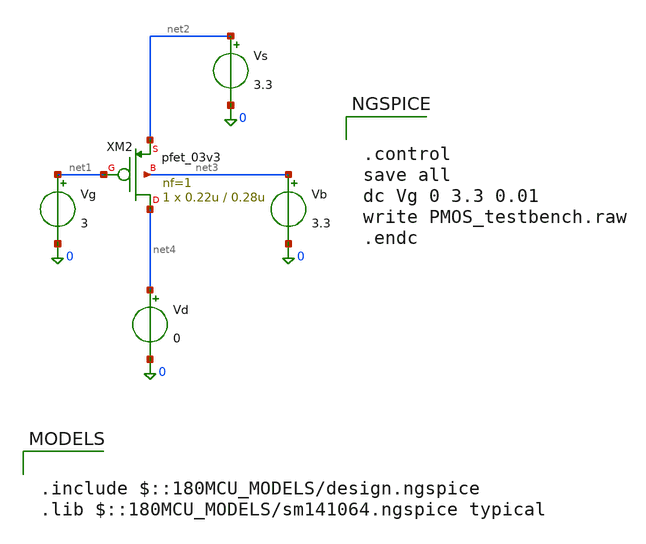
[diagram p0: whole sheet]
** sch_path: 3_Examples/FET_Characterization/PMOS_testbench.sch
**.subckt PMOS_testbench
Vg net1 0 3
Vd net4 0 0
Vb net3 0 3.3
Vs net2 0 3.3
XM2 net4 net1 net2 net3 pfet_03v3 L=0.28u W=0.22u nf=1 ad='int((nf+1)/2) * W/nf * 0.18u' as='int((nf+2)/2) * W/nf * 0.18u'
+ pd='2*int((nf+1)/2) * (W/nf + 0.18u)' ps='2*int((nf+2)/2) * (W/nf + 0.18u)' nrd='0.18u / W' nrs='0.18u / W'
+ sa=0 sb=0 sd=0 m=1 par=1
**** begin user architecture code

.include $::180MCU_MODELS/design.ngspice
.lib $::180MCU_MODELS/sm141064.ngspice typical



.control
save all
dc Vg 0 3.3 0.01
write PMOS_testbench.raw
.endc


**** end user architecture code
**.ends
.end
